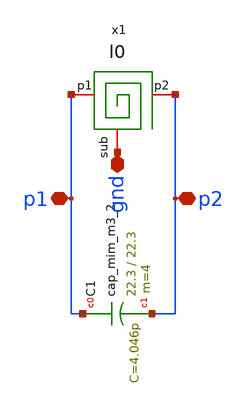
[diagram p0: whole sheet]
** sch_path: examples/sq_1nH_2.5GHz/xschem/lc.sch
**.subckt lc p1 p2 gnd
*.iopin p1
*.iopin p2
*.iopin gnd
x1 p1 p2 gnd l0
XC1 p1 p2 sky130_fd_pr__cap_mim_m3_2 W=22.3 L=22.3 MF=4 m=4
**.ends

* expanding   symbol:  /foss/designs/asitic-example/examples/sq_1nH_2.5GHz/xschem/l0.sym # of pins=3
** sym_path: examples/sq_1nH_2.5GHz/xschem/l0.sym
** sch_path: examples/sq_1nH_2.5GHz/xschem/l0.sch
.subckt l0 p1 p2 sub
*.iopin sub
*.iopin p1
*.iopin p2
R net2 p2 2.857 m=1
L p1 net2 1.006n m=1
Rs1 net1 sub 27.37 m=1
Cs1 p1 net1 33.97f m=1
Cs2 p2 net3 36.78f m=1
Rs2 net3 sub -9 m=1
.ends

.end
